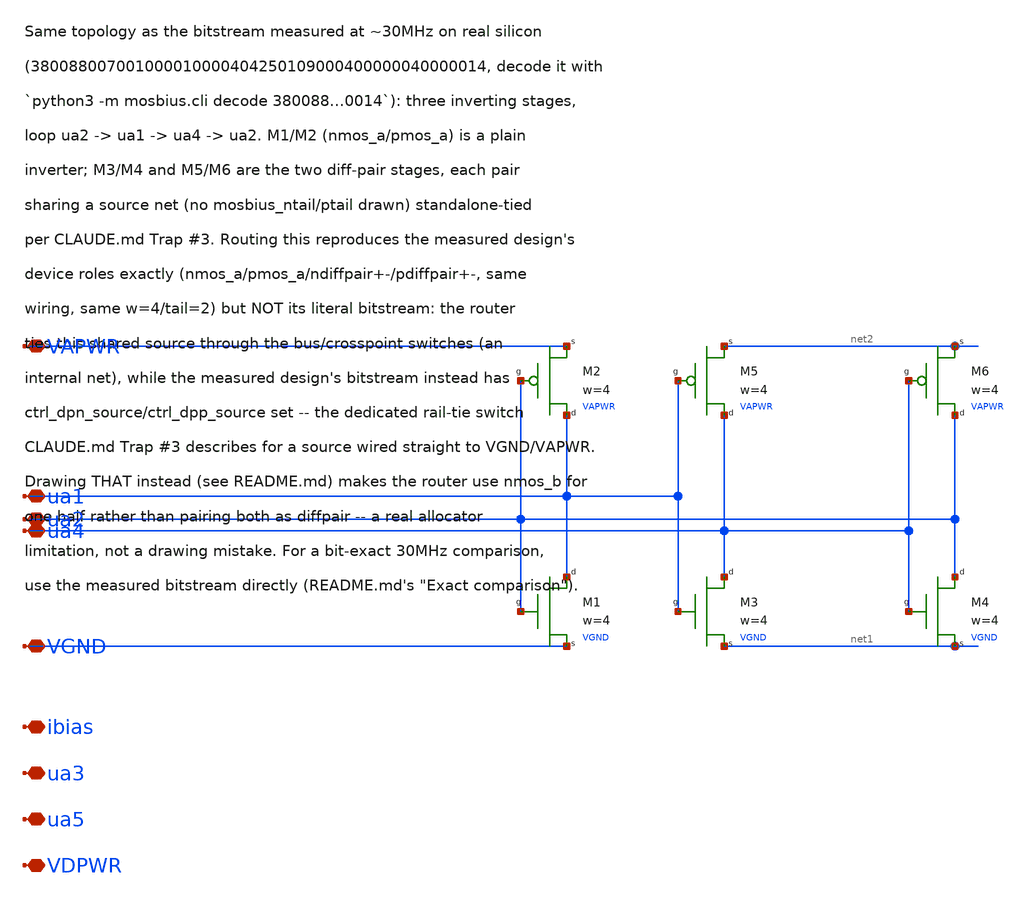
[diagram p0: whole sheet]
** sch_path: examples/ringosc/ring.sch
**.subckt ring ua1 ua2 ua4 VGND VAPWR ibias ua3 ua5 VDPWR
*.iopin ua1
*.iopin ua2
*.iopin ua4
*.iopin VGND
*.iopin VAPWR
*.iopin ibias
*.iopin ua3
*.iopin ua5
*.iopin VDPWR
XM1 ua2 ua1 VGND VGND mosbius_nmos w=4
M2 ua2 ua1 VAPWR VAPWR mosbius_pmos w=4
XM3 ua1 ua4 net1 VGND mosbius_nmos w=4
XM4 ua4 ua2 net1 VGND mosbius_nmos w=4
M5 ua1 ua4 net2 VAPWR mosbius_pmos w=4
M6 ua4 ua2 net2 VAPWR mosbius_pmos w=4
**.ends

* expanding   symbol:  mosbius_nmos.sym # of pins=3
** sym_path: xschem/mosbius_lib/mosbius_nmos.sym
** sch_path: xschem/mosbius_lib/mosbius_nmos.sch
.subckt mosbius_nmos g d s b  w=1
*.iopin s
*.ipin g
*.iopin d
XM1 d g s well sky130_fd_pr__nfet_g5v0d10v5 L=0.5 W=wdev nf=nfdev ad='int((nf+1)/2) * W/nf * 0.29' as='int((nf+2)/2) * W/nf * 0.29'
+ pd='2*int((nf+1)/2) * (W/nf + 0.29)' ps='2*int((nf+2)/2) * (W/nf + 0.29)' nrd='0.29 / W' nrs='0.29 / W'
+ sa=0 sb=0 sd=0 mult=1 m=1
**** begin user architecture code

.param wdev='10*w' nfdev='2*w'

**** end user architecture code
Rwell_source well s 'rwell_source' m=1
Rwell_rail well b 'rwell_rail' m=1
* implicit port xxx
.ends


* expanding   symbol:  mosbius_pmos.sym # of pins=3
** sym_path: xschem/mosbius_lib/mosbius_pmos.sym
** sch_path: xschem/mosbius_lib/mosbius_pmos.sch
.subckt mosbius_pmos g d s b  w=1
*.iopin s
*.ipin g
*.iopin d
XM1 d g s well sky130_fd_pr__pfet_g5v0d10v5 L=0.5 W=wdev nf=nfdev ad='int((nf+1)/2) * W/nf * 0.29' as='int((nf+2)/2) * W/nf * 0.29'
+ pd='2*int((nf+1)/2) * (W/nf + 0.29)' ps='2*int((nf+2)/2) * (W/nf + 0.29)' nrd='0.29 / W' nrs='0.29 / W'
+ sa=0 sb=0 sd=0 mult=1 m=1
**** begin user architecture code

.param wdev='30*w' nfdev='wdev/pmos_width_per_finger'

**** end user architecture code
Rwell_source well s 'rwell_source' m=1
Rwell_rail well b 'rwell_rail' m=1
* implicit port xxx
.ends

.end
